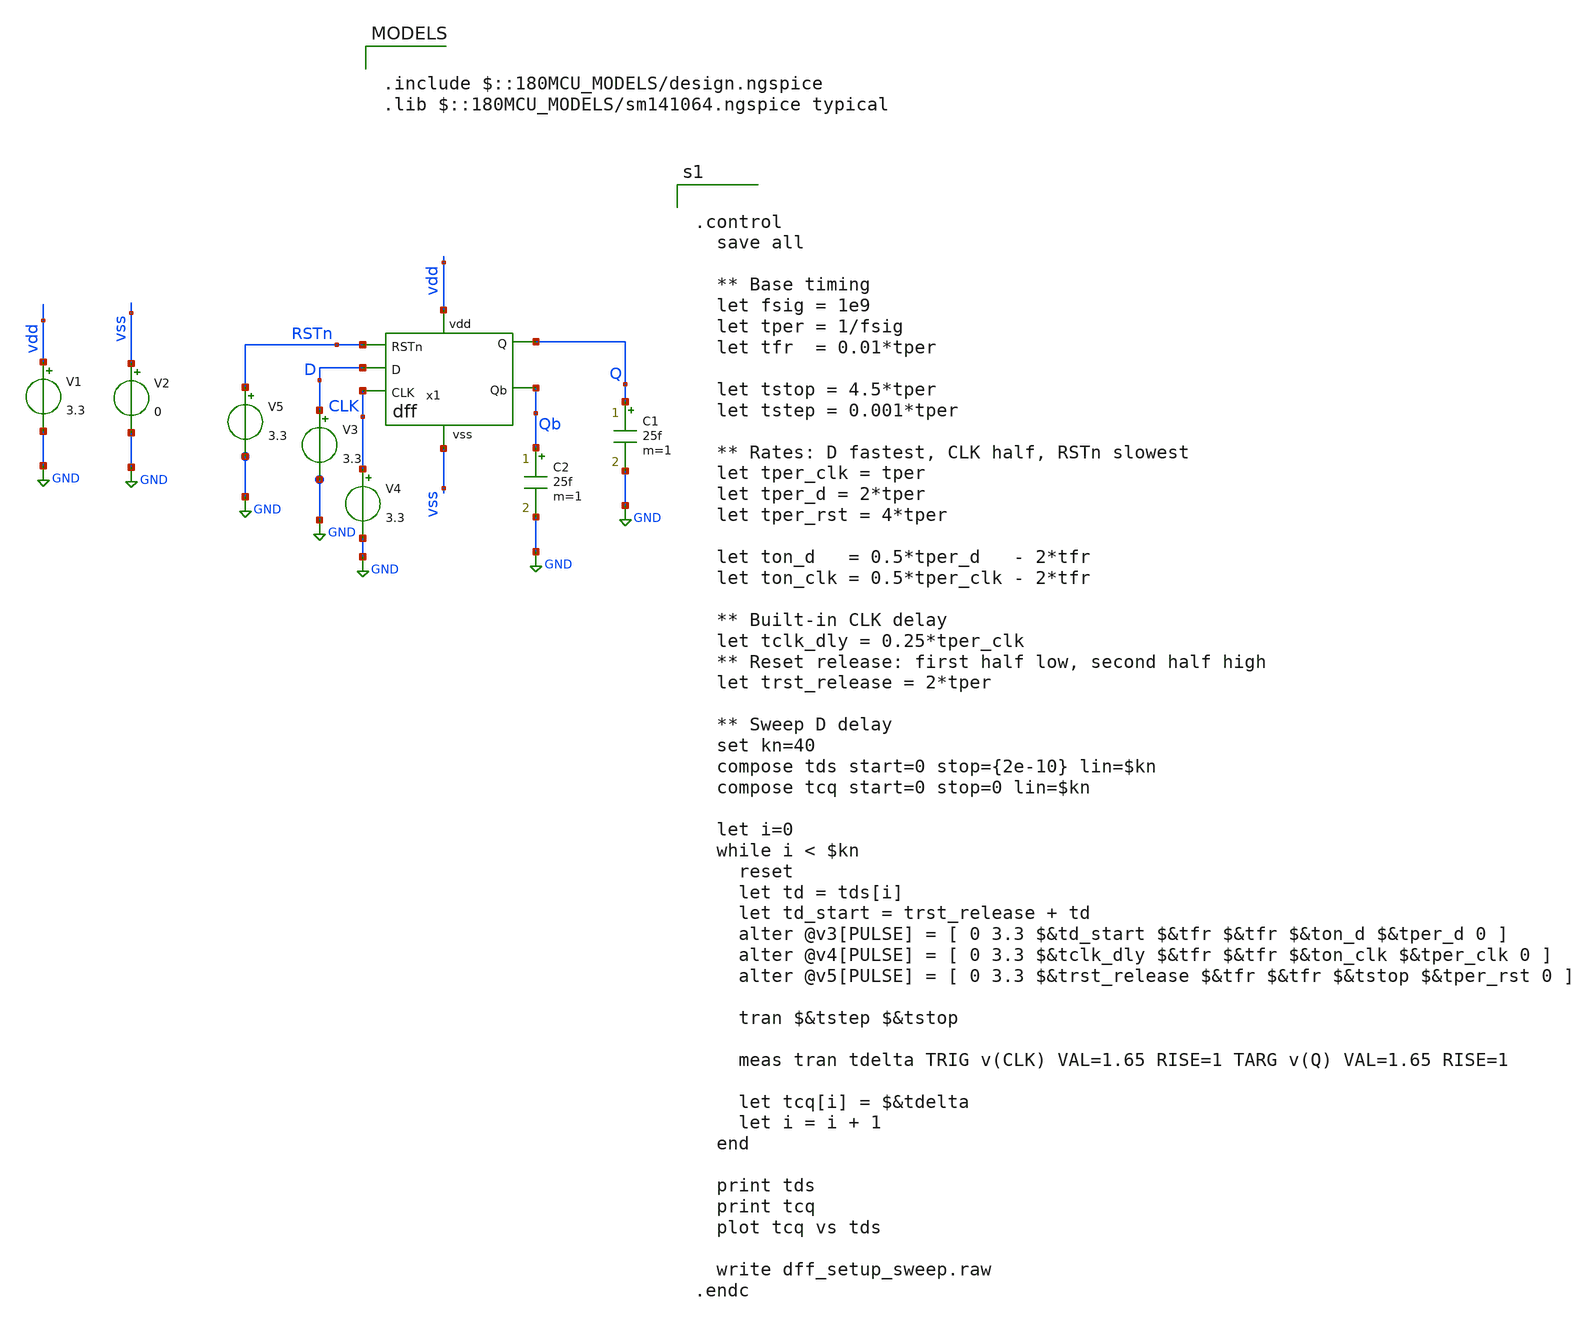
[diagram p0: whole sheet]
** sch_path: dff_measure.sch
**.subckt dff_measure
V1 vdd GND 3.3
V2 vss GND 0
V3 D GND 3.3
C1 Q GND 25f m=1
V4 CLK GND 3.3
x1 RSTn D Q Qb CLK vdd vss dff
C2 Qb GND 25f m=1
V5 RSTn GND 3.3
**** begin user architecture code

.include $::180MCU_MODELS/design.ngspice
.lib $::180MCU_MODELS/sm141064.ngspice typical



.control
  save all

  ** Base timing
  let fsig = 1e9
  let tper = 1/fsig
  let tfr  = 0.01*tper

  let tstop = 4.5*tper
  let tstep = 0.001*tper

  ** Rates: D fastest, CLK half, RSTn slowest
  let tper_clk = tper
  let tper_d = 2*tper
  let tper_rst = 4*tper

  let ton_d   = 0.5*tper_d   - 2*tfr
  let ton_clk = 0.5*tper_clk - 2*tfr

  ** Built-in CLK delay
  let tclk_dly = 0.25*tper_clk
  ** Reset release: first half low, second half high
  let trst_release = 2*tper

  ** Sweep D delay
  set kn=40
  compose tds start=0 stop={2e-10} lin=$kn
  compose tcq start=0 stop=0 lin=$kn

  let i=0
  while i < $kn
    reset
    let td = tds[i]
    let td_start = trst_release + td
    alter @v3[PULSE] = [ 0 3.3 $&td_start $&tfr $&tfr $&ton_d $&tper_d 0 ]
    alter @v4[PULSE] = [ 0 3.3 $&tclk_dly $&tfr $&tfr $&ton_clk $&tper_clk 0 ]
    alter @v5[PULSE] = [ 0 3.3 $&trst_release $&tfr $&tfr $&tstop $&tper_rst 0 ]

    tran $&tstep $&tstop

    meas tran tdelta TRIG v(CLK) VAL=1.65 RISE=1 TARG v(Q) VAL=1.65 RISE=1

    let tcq[i] = $&tdelta
    let i = i + 1
  end

  print tds
  print tcq
  plot tcq vs tds

  write dff_setup_sweep.raw
.endc


**** end user architecture code
**.ends

* expanding   symbol:  dff.sym # of pins=7
** sym_path: dff.sym
** sch_path: dff.sch
.subckt dff RSTn D Q Qb CLK vdd vss
*.ipin CLK
*.ipin RSTn
*.opin Qb
*.opin Q
*.ipin D
*.iopin vdd
*.iopin vss
x1 Dn vdd cbar c vss net1 tgate
x4 vdd net1 net2 RSTn vss nand2
x3 vdd Dn net2 vss inv
x5 net2 vdd cbar c vss net5 tgate
x6 vdd net3 net5 RSTn vss nand2
x7 vdd c net5 net3 cbar vss tristate
x8 vdd net3 Q vss inv
x9 vdd net3 net4 vss inv
x10 vdd net4 Qb vss inv
x11 vdd CLK cbar vss inv
x12 vdd cbar c vss inv
x13 vdd c Dn D cbar vss tristate
.ends


* expanding   symbol:  tgate.sym # of pins=6
** sym_path: tgate.sym
** sch_path: tgate.sch
.subckt tgate in vdd cbar c vss out
*.ipin in
*.opin out
*.ipin cbar
*.ipin c
*.iopin vdd
*.iopin vss
XM1 out cbar in vdd pfet_03v3 L=0.28u W=0.42u nf=1 ad='int((nf+1)/2) * W/nf * 0.18u' as='int((nf+2)/2) * W/nf * 0.18u'
+ pd='2*int((nf+1)/2) * (W/nf + 0.18u)' ps='2*int((nf+2)/2) * (W/nf + 0.18u)' nrd='0.18u / W' nrs='0.18u / W'
+ sa=0 sb=0 sd=0 m=1
XM2 out c in vss nfet_03v3 L=0.28u W=0.42u nf=1 ad='int((nf+1)/2) * W/nf * 0.18u' as='int((nf+2)/2) * W/nf * 0.18u'
+ pd='2*int((nf+1)/2) * (W/nf + 0.18u)' ps='2*int((nf+2)/2) * (W/nf + 0.18u)' nrd='0.18u / W' nrs='0.18u / W'
+ sa=0 sb=0 sd=0 m=1
.ends


* expanding   symbol:  nand2.sym # of pins=5
** sym_path: nand2.sym
** sch_path: nand2.sch
.subckt nand2 vdd OUT IN0 IN1 vss
*.ipin IN0
*.ipin IN1
*.opin OUT
*.iopin vdd
*.iopin vss
XM1 net1 IN1 vss vss nfet_03v3 L=0.28u W=1u nf=1 ad='int((nf+1)/2) * W/nf * 0.18u' as='int((nf+2)/2) * W/nf * 0.18u'
+ pd='2*int((nf+1)/2) * (W/nf + 0.18u)' ps='2*int((nf+2)/2) * (W/nf + 0.18u)' nrd='0.18u / W' nrs='0.18u / W'
+ sa=0 sb=0 sd=0 m=1
XM3 OUT IN0 vdd vdd pfet_03v3 L=0.28u W=1u nf=1 ad='int((nf+1)/2) * W/nf * 0.18u' as='int((nf+2)/2) * W/nf * 0.18u'
+ pd='2*int((nf+1)/2) * (W/nf + 0.18u)' ps='2*int((nf+2)/2) * (W/nf + 0.18u)' nrd='0.18u / W' nrs='0.18u / W'
+ sa=0 sb=0 sd=0 m=1
XM4 OUT IN1 vdd vdd pfet_03v3 L=0.28u W=1u nf=1 ad='int((nf+1)/2) * W/nf * 0.18u' as='int((nf+2)/2) * W/nf * 0.18u'
+ pd='2*int((nf+1)/2) * (W/nf + 0.18u)' ps='2*int((nf+2)/2) * (W/nf + 0.18u)' nrd='0.18u / W' nrs='0.18u / W'
+ sa=0 sb=0 sd=0 m=1
XM2 OUT IN0 net1 vss nfet_03v3 L=0.28u W=1u nf=1 ad='int((nf+1)/2) * W/nf * 0.18u' as='int((nf+2)/2) * W/nf * 0.18u'
+ pd='2*int((nf+1)/2) * (W/nf + 0.18u)' ps='2*int((nf+2)/2) * (W/nf + 0.18u)' nrd='0.18u / W' nrs='0.18u / W'
+ sa=0 sb=0 sd=0 m=1
.ends


* expanding   symbol:  inv.sym # of pins=4
** sym_path: inv.sym
** sch_path: inv.sch
.subckt inv vdd IN OUT vss
*.ipin IN
*.opin OUT
*.iopin vdd
*.iopin vss
XM1 OUT IN vss vss nfet_03v3 L=0.28u W=1u nf=1 ad='int((nf+1)/2) * W/nf * 0.18u' as='int((nf+2)/2) * W/nf * 0.18u'
+ pd='2*int((nf+1)/2) * (W/nf + 0.18u)' ps='2*int((nf+2)/2) * (W/nf + 0.18u)' nrd='0.18u / W' nrs='0.18u / W'
+ sa=0 sb=0 sd=0 m=1
XM2 OUT IN vdd vdd pfet_03v3 L=0.28u W=1u nf=1 ad='int((nf+1)/2) * W/nf * 0.18u' as='int((nf+2)/2) * W/nf * 0.18u'
+ pd='2*int((nf+1)/2) * (W/nf + 0.18u)' ps='2*int((nf+2)/2) * (W/nf + 0.18u)' nrd='0.18u / W' nrs='0.18u / W'
+ sa=0 sb=0 sd=0 m=1
.ends


* expanding   symbol:  tristate.sym # of pins=6
** sym_path: tristate.sym
** sch_path: tristate.sch
.subckt tristate vdd c out in cbar vss
*.ipin in
*.opin out
*.iopin vdd
*.iopin vss
*.ipin c
*.ipin cbar
XM1 net1 c vdd vdd pfet_03v3 L=0.28u W=0.42u nf=1 ad='int((nf+1)/2) * W/nf * 0.18u' as='int((nf+2)/2) * W/nf * 0.18u'
+ pd='2*int((nf+1)/2) * (W/nf + 0.18u)' ps='2*int((nf+2)/2) * (W/nf + 0.18u)' nrd='0.18u / W' nrs='0.18u / W'
+ sa=0 sb=0 sd=0 m=1
XM2 out in net1 vdd pfet_03v3 L=0.28u W=0.42u nf=1 ad='int((nf+1)/2) * W/nf * 0.18u' as='int((nf+2)/2) * W/nf * 0.18u'
+ pd='2*int((nf+1)/2) * (W/nf + 0.18u)' ps='2*int((nf+2)/2) * (W/nf + 0.18u)' nrd='0.18u / W' nrs='0.18u / W'
+ sa=0 sb=0 sd=0 m=1
XM3 out in net2 vss nfet_03v3 L=0.28u W=0.42u nf=1 ad='int((nf+1)/2) * W/nf * 0.18u' as='int((nf+2)/2) * W/nf * 0.18u'
+ pd='2*int((nf+1)/2) * (W/nf + 0.18u)' ps='2*int((nf+2)/2) * (W/nf + 0.18u)' nrd='0.18u / W' nrs='0.18u / W'
+ sa=0 sb=0 sd=0 m=1
XM4 net2 cbar vss vss nfet_03v3 L=0.28u W=0.42u nf=1 ad='int((nf+1)/2) * W/nf * 0.18u' as='int((nf+2)/2) * W/nf * 0.18u'
+ pd='2*int((nf+1)/2) * (W/nf + 0.18u)' ps='2*int((nf+2)/2) * (W/nf + 0.18u)' nrd='0.18u / W' nrs='0.18u / W'
+ sa=0 sb=0 sd=0 m=1
.ends

.GLOBAL GND
.end
